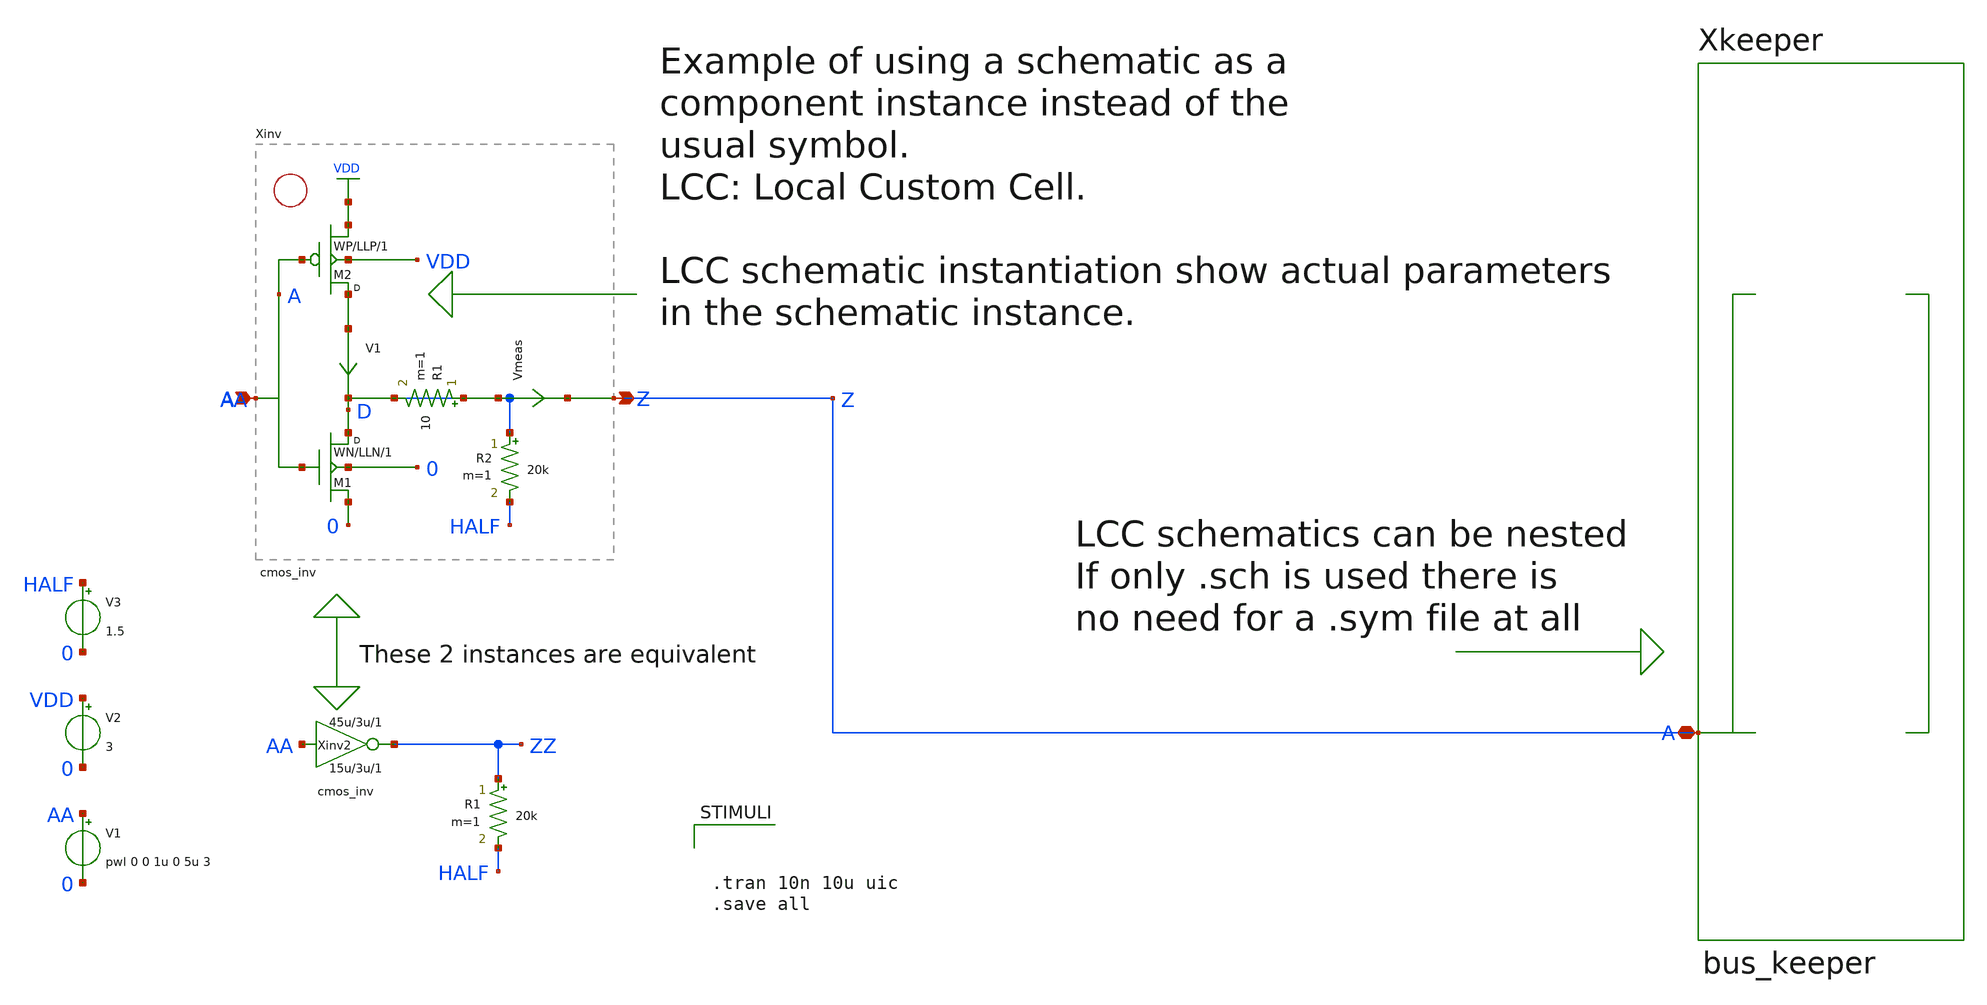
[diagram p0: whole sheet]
** sch_path: xschem_library/examples/LCC_instances.sch
**.subckt LCC_instances
V1 AA 0 pwl 0 0 1u 0 5u 3
V2 VDD 0 3
R1 ZZ HALF 20k m=1
V3 HALF 0 1.5
R2 Z HALF 20k m=1
Xinv Z AA cmos_inv WN=15u WP=45u LLN=3u LLP=3u m=1
Xinv2 ZZ AA cmos_inv WN=15u WP=45u LLN=3u LLP=3u m=1
Xkeeper Z bus_keeper WN_FB=3u WP_FB=4u
**** begin user architecture code



.tran 10n 10u uic
.save all



************************************************
*         NOMINAL N-Channel Transistor         *
*            UCB-3 Parameter Set               *
*         HIGH-SPEED CMOS Logic Family         *
*                10-Jan.-1995                  *
************************************************
.Model N NMOS ( LEVEL = 3 KP    = 45.3E-6 VTO   = 0.72 TOX   = 51.5E-9 NSUB  = 2.8E15 GAMMA = 0.94
+ PHI   = 0.65 VMAX  = 150E3 RS    = 40 RD    = 40 XJ    = 0.11E-6 LD    = 0.52E-6 DELTA = 0.315 THETA =
+ 0.054 ETA   = 0.025 KAPPA = 0.0 WD    = 0.0 )

***********************************************
*        NOMINAL P-Channel transistor         *
*           UCB-3 Parameter Set               *
*         HIGH-SPEED CMOS Logic Family        *
*               10-Jan.-1995                  *
***********************************************
.Model P PMOS ( LEVEL = 3 KP    = 22.1E-6 VTO   = -0.71 TOX   = 51.5E-9 NSUB  = 3.3E16 GAMMA = 0.92
+ PHI   = 0.65 VMAX  = 970E3 RS    = 80 RD    = 80 XJ    = 0.63E-6 LD    = 0.23E-6 DELTA = 2.24 THETA =
+ 0.108 ETA   = 0.322 KAPPA = 0.0 WD    = 0.0 )





**** end user architecture code
**.ends
.end
